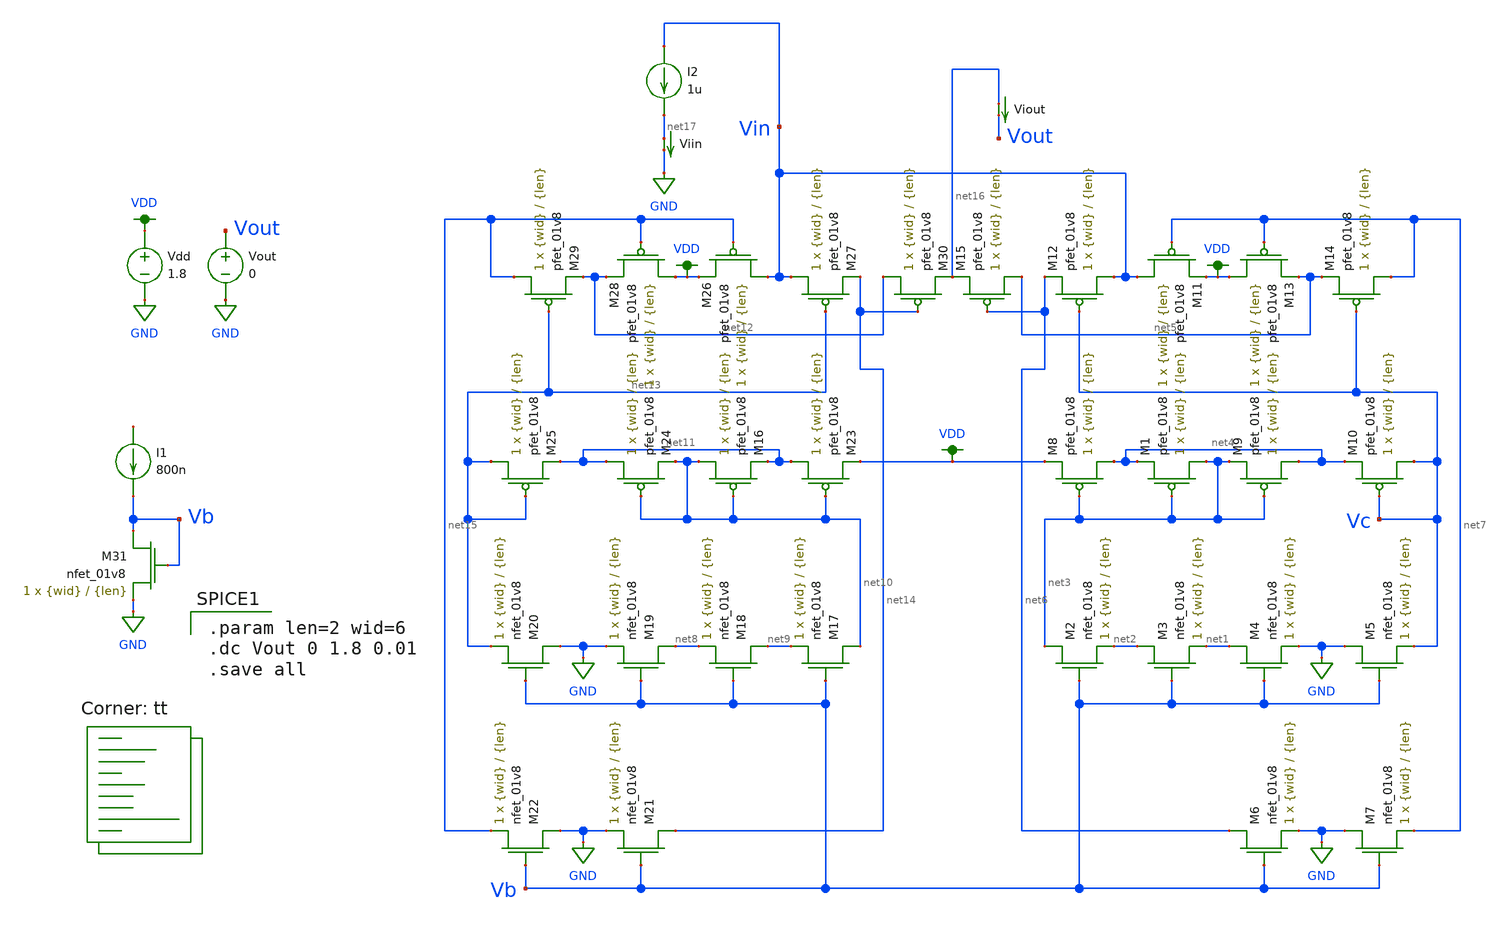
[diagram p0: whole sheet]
** sch_path: mp3/mirror_lvs_tb.sch
**.subckt mirror_lvs_tb
XM1 net3 net3 net4 VDD sky130_fd_pr__pfet_01v8 L={len} W={wid} nf=1 ad='int((nf+1)/2) * W/nf * 0.29'
+ as='int((nf+2)/2) * W/nf * 0.29' pd='2*int((nf+1)/2) * (W/nf + 0.29)' ps='2*int((nf+2)/2) * (W/nf + 0.29)'
+ nrd='0.29 / W' nrs='0.29 / W' sa=0 sb=0 sd=0 mult=1 m=1
XM2 net3 Vb net2 GND sky130_fd_pr__nfet_01v8 L={len} W={wid} nf=1 ad='int((nf+1)/2) * W/nf * 0.29' as='int((nf+2)/2) * W/nf * 0.29'
+ pd='2*int((nf+1)/2) * (W/nf + 0.29)' ps='2*int((nf+2)/2) * (W/nf + 0.29)' nrd='0.29 / W' nrs='0.29 / W'
+ sa=0 sb=0 sd=0 mult=1 m=1
XM3 net2 Vb net1 GND sky130_fd_pr__nfet_01v8 L={len} W={wid} nf=1 ad='int((nf+1)/2) * W/nf * 0.29' as='int((nf+2)/2) * W/nf * 0.29'
+ pd='2*int((nf+1)/2) * (W/nf + 0.29)' ps='2*int((nf+2)/2) * (W/nf + 0.29)' nrd='0.29 / W' nrs='0.29 / W'
+ sa=0 sb=0 sd=0 mult=1 m=1
XM4 net1 Vb GND GND sky130_fd_pr__nfet_01v8 L={len} W={wid} nf=1 ad='int((nf+1)/2) * W/nf * 0.29' as='int((nf+2)/2) * W/nf * 0.29'
+ pd='2*int((nf+1)/2) * (W/nf + 0.29)' ps='2*int((nf+2)/2) * (W/nf + 0.29)' nrd='0.29 / W' nrs='0.29 / W'
+ sa=0 sb=0 sd=0 mult=1 m=1
XM5 GND Vb Vc GND sky130_fd_pr__nfet_01v8 L={len} W={wid} nf=1 ad='int((nf+1)/2) * W/nf * 0.29' as='int((nf+2)/2) * W/nf * 0.29'
+ pd='2*int((nf+1)/2) * (W/nf + 0.29)' ps='2*int((nf+2)/2) * (W/nf + 0.29)' nrd='0.29 / W' nrs='0.29 / W'
+ sa=0 sb=0 sd=0 mult=1 m=1
XM6 net6 Vb GND GND sky130_fd_pr__nfet_01v8 L={len} W={wid} nf=1 ad='int((nf+1)/2) * W/nf * 0.29' as='int((nf+2)/2) * W/nf * 0.29'
+ pd='2*int((nf+1)/2) * (W/nf + 0.29)' ps='2*int((nf+2)/2) * (W/nf + 0.29)' nrd='0.29 / W' nrs='0.29 / W'
+ sa=0 sb=0 sd=0 mult=1 m=1
XM7 GND Vb net7 GND sky130_fd_pr__nfet_01v8 L={len} W={wid} nf=1 ad='int((nf+1)/2) * W/nf * 0.29' as='int((nf+2)/2) * W/nf * 0.29'
+ pd='2*int((nf+1)/2) * (W/nf + 0.29)' ps='2*int((nf+2)/2) * (W/nf + 0.29)' nrd='0.29 / W' nrs='0.29 / W'
+ sa=0 sb=0 sd=0 mult=1 m=1
XM8 net4 net3 VDD VDD sky130_fd_pr__pfet_01v8 L={len} W={wid} nf=1 ad='int((nf+1)/2) * W/nf * 0.29' as='int((nf+2)/2) * W/nf * 0.29'
+ pd='2*int((nf+1)/2) * (W/nf + 0.29)' ps='2*int((nf+2)/2) * (W/nf + 0.29)' nrd='0.29 / W' nrs='0.29 / W'
+ sa=0 sb=0 sd=0 mult=1 m=1
XM9 net4 net3 net3 VDD sky130_fd_pr__pfet_01v8 L={len} W={wid} nf=1 ad='int((nf+1)/2) * W/nf * 0.29'
+ as='int((nf+2)/2) * W/nf * 0.29' pd='2*int((nf+1)/2) * (W/nf + 0.29)' ps='2*int((nf+2)/2) * (W/nf + 0.29)'
+ nrd='0.29 / W' nrs='0.29 / W' sa=0 sb=0 sd=0 mult=1 m=1
XM10 Vc Vc net4 VDD sky130_fd_pr__pfet_01v8 L={len} W={wid} nf=1 ad='int((nf+1)/2) * W/nf * 0.29' as='int((nf+2)/2) * W/nf * 0.29'
+ pd='2*int((nf+1)/2) * (W/nf + 0.29)' ps='2*int((nf+2)/2) * (W/nf + 0.29)' nrd='0.29 / W' nrs='0.29 / W'
+ sa=0 sb=0 sd=0 mult=1 m=1
XM11 Vin net7 VDD VDD sky130_fd_pr__pfet_01v8 L={len} W={wid} nf=1 ad='int((nf+1)/2) * W/nf * 0.29' as='int((nf+2)/2) * W/nf * 0.29'
+ pd='2*int((nf+1)/2) * (W/nf + 0.29)' ps='2*int((nf+2)/2) * (W/nf + 0.29)' nrd='0.29 / W' nrs='0.29 / W'
+ sa=0 sb=0 sd=0 mult=1 m=1
XM12 Vin Vc net6 VDD sky130_fd_pr__pfet_01v8 L={len} W={wid} nf=1 ad='int((nf+1)/2) * W/nf * 0.29' as='int((nf+2)/2) * W/nf * 0.29'
+ pd='2*int((nf+1)/2) * (W/nf + 0.29)' ps='2*int((nf+2)/2) * (W/nf + 0.29)' nrd='0.29 / W' nrs='0.29 / W'
+ sa=0 sb=0 sd=0 mult=1 m=1
XM13 VDD net7 net5 VDD sky130_fd_pr__pfet_01v8 L={len} W={wid} nf=1 ad='int((nf+1)/2) * W/nf * 0.29'
+ as='int((nf+2)/2) * W/nf * 0.29' pd='2*int((nf+1)/2) * (W/nf + 0.29)' ps='2*int((nf+2)/2) * (W/nf + 0.29)'
+ nrd='0.29 / W' nrs='0.29 / W' sa=0 sb=0 sd=0 mult=1 m=1
XM14 net7 Vc net5 VDD sky130_fd_pr__pfet_01v8 L={len} W={wid} nf=1 ad='int((nf+1)/2) * W/nf * 0.29' as='int((nf+2)/2) * W/nf * 0.29'
+ pd='2*int((nf+1)/2) * (W/nf + 0.29)' ps='2*int((nf+2)/2) * (W/nf + 0.29)' nrd='0.29 / W' nrs='0.29 / W'
+ sa=0 sb=0 sd=0 mult=1 m=1
XM15 net5 net6 net16 VDD sky130_fd_pr__pfet_01v8 L={len} W={wid} nf=1 ad='int((nf+1)/2) * W/nf * 0.29'
+ as='int((nf+2)/2) * W/nf * 0.29' pd='2*int((nf+1)/2) * (W/nf + 0.29)' ps='2*int((nf+2)/2) * (W/nf + 0.29)'
+ nrd='0.29 / W' nrs='0.29 / W' sa=0 sb=0 sd=0 mult=1 m=1
XM16 net10 net10 net11 VDD sky130_fd_pr__pfet_01v8 L={len} W={wid} nf=1 ad='int((nf+1)/2) * W/nf * 0.29'
+ as='int((nf+2)/2) * W/nf * 0.29' pd='2*int((nf+1)/2) * (W/nf + 0.29)' ps='2*int((nf+2)/2) * (W/nf + 0.29)'
+ nrd='0.29 / W' nrs='0.29 / W' sa=0 sb=0 sd=0 mult=1 m=1
XM17 net10 Vb net9 GND sky130_fd_pr__nfet_01v8 L={len} W={wid} nf=1 ad='int((nf+1)/2) * W/nf * 0.29'
+ as='int((nf+2)/2) * W/nf * 0.29' pd='2*int((nf+1)/2) * (W/nf + 0.29)' ps='2*int((nf+2)/2) * (W/nf + 0.29)'
+ nrd='0.29 / W' nrs='0.29 / W' sa=0 sb=0 sd=0 mult=1 m=1
XM18 net9 Vb net8 GND sky130_fd_pr__nfet_01v8 L={len} W={wid} nf=1 ad='int((nf+1)/2) * W/nf * 0.29' as='int((nf+2)/2) * W/nf * 0.29'
+ pd='2*int((nf+1)/2) * (W/nf + 0.29)' ps='2*int((nf+2)/2) * (W/nf + 0.29)' nrd='0.29 / W' nrs='0.29 / W'
+ sa=0 sb=0 sd=0 mult=1 m=1
XM19 net8 Vb GND GND sky130_fd_pr__nfet_01v8 L={len} W={wid} nf=1 ad='int((nf+1)/2) * W/nf * 0.29' as='int((nf+2)/2) * W/nf * 0.29'
+ pd='2*int((nf+1)/2) * (W/nf + 0.29)' ps='2*int((nf+2)/2) * (W/nf + 0.29)' nrd='0.29 / W' nrs='0.29 / W'
+ sa=0 sb=0 sd=0 mult=1 m=1
XM20 GND Vb net13 GND sky130_fd_pr__nfet_01v8 L={len} W={wid} nf=1 ad='int((nf+1)/2) * W/nf * 0.29' as='int((nf+2)/2) * W/nf * 0.29'
+ pd='2*int((nf+1)/2) * (W/nf + 0.29)' ps='2*int((nf+2)/2) * (W/nf + 0.29)' nrd='0.29 / W' nrs='0.29 / W'
+ sa=0 sb=0 sd=0 mult=1 m=1
XM21 net14 Vb GND GND sky130_fd_pr__nfet_01v8 L={len} W={wid} nf=1 ad='int((nf+1)/2) * W/nf * 0.29' as='int((nf+2)/2) * W/nf * 0.29'
+ pd='2*int((nf+1)/2) * (W/nf + 0.29)' ps='2*int((nf+2)/2) * (W/nf + 0.29)' nrd='0.29 / W' nrs='0.29 / W'
+ sa=0 sb=0 sd=0 mult=1 m=1
XM22 GND Vb net15 GND sky130_fd_pr__nfet_01v8 L={len} W={wid} nf=1 ad='int((nf+1)/2) * W/nf * 0.29' as='int((nf+2)/2) * W/nf * 0.29'
+ pd='2*int((nf+1)/2) * (W/nf + 0.29)' ps='2*int((nf+2)/2) * (W/nf + 0.29)' nrd='0.29 / W' nrs='0.29 / W'
+ sa=0 sb=0 sd=0 mult=1 m=1
XM23 net11 net10 VDD VDD sky130_fd_pr__pfet_01v8 L={len} W={wid} nf=1 ad='int((nf+1)/2) * W/nf * 0.29'
+ as='int((nf+2)/2) * W/nf * 0.29' pd='2*int((nf+1)/2) * (W/nf + 0.29)' ps='2*int((nf+2)/2) * (W/nf + 0.29)'
+ nrd='0.29 / W' nrs='0.29 / W' sa=0 sb=0 sd=0 mult=1 m=1
XM24 net11 net10 net10 VDD sky130_fd_pr__pfet_01v8 L={len} W={wid} nf=1 ad='int((nf+1)/2) * W/nf * 0.29'
+ as='int((nf+2)/2) * W/nf * 0.29' pd='2*int((nf+1)/2) * (W/nf + 0.29)' ps='2*int((nf+2)/2) * (W/nf + 0.29)'
+ nrd='0.29 / W' nrs='0.29 / W' sa=0 sb=0 sd=0 mult=1 m=1
XM25 net13 net13 net11 VDD sky130_fd_pr__pfet_01v8 L={len} W={wid} nf=1 ad='int((nf+1)/2) * W/nf * 0.29'
+ as='int((nf+2)/2) * W/nf * 0.29' pd='2*int((nf+1)/2) * (W/nf + 0.29)' ps='2*int((nf+2)/2) * (W/nf + 0.29)'
+ nrd='0.29 / W' nrs='0.29 / W' sa=0 sb=0 sd=0 mult=1 m=1
XM26 Vin net15 VDD VDD sky130_fd_pr__pfet_01v8 L={len} W={wid} nf=1 ad='int((nf+1)/2) * W/nf * 0.29'
+ as='int((nf+2)/2) * W/nf * 0.29' pd='2*int((nf+1)/2) * (W/nf + 0.29)' ps='2*int((nf+2)/2) * (W/nf + 0.29)'
+ nrd='0.29 / W' nrs='0.29 / W' sa=0 sb=0 sd=0 mult=1 m=1
XM27 Vin net13 net14 VDD sky130_fd_pr__pfet_01v8 L={len} W={wid} nf=1 ad='int((nf+1)/2) * W/nf * 0.29'
+ as='int((nf+2)/2) * W/nf * 0.29' pd='2*int((nf+1)/2) * (W/nf + 0.29)' ps='2*int((nf+2)/2) * (W/nf + 0.29)'
+ nrd='0.29 / W' nrs='0.29 / W' sa=0 sb=0 sd=0 mult=1 m=1
XM28 VDD net15 net12 VDD sky130_fd_pr__pfet_01v8 L={len} W={wid} nf=1 ad='int((nf+1)/2) * W/nf * 0.29'
+ as='int((nf+2)/2) * W/nf * 0.29' pd='2*int((nf+1)/2) * (W/nf + 0.29)' ps='2*int((nf+2)/2) * (W/nf + 0.29)'
+ nrd='0.29 / W' nrs='0.29 / W' sa=0 sb=0 sd=0 mult=1 m=1
XM29 net15 net13 net12 VDD sky130_fd_pr__pfet_01v8 L={len} W={wid} nf=1 ad='int((nf+1)/2) * W/nf * 0.29'
+ as='int((nf+2)/2) * W/nf * 0.29' pd='2*int((nf+1)/2) * (W/nf + 0.29)' ps='2*int((nf+2)/2) * (W/nf + 0.29)'
+ nrd='0.29 / W' nrs='0.29 / W' sa=0 sb=0 sd=0 mult=1 m=1
XM30 net12 net14 net16 VDD sky130_fd_pr__pfet_01v8 L={len} W={wid} nf=1 ad='int((nf+1)/2) * W/nf * 0.29'
+ as='int((nf+2)/2) * W/nf * 0.29' pd='2*int((nf+1)/2) * (W/nf + 0.29)' ps='2*int((nf+2)/2) * (W/nf + 0.29)'
+ nrd='0.29 / W' nrs='0.29 / W' sa=0 sb=0 sd=0 mult=1 m=1
Vdd VDD GND 1.8
I1 net18 Vb 800n
XM31 Vb Vb GND GND sky130_fd_pr__nfet_01v8 L={len} W={wid} nf=1 ad='int((nf+1)/2) * W/nf * 0.29' as='int((nf+2)/2) * W/nf * 0.29'
+ pd='2*int((nf+1)/2) * (W/nf + 0.29)' ps='2*int((nf+2)/2) * (W/nf + 0.29)' nrd='0.29 / W' nrs='0.29 / W'
+ sa=0 sb=0 sd=0 mult=1 m=1
I2 Vin net17 1u
Vout Vout GND 0
Viout net16 Vout 0
.save i(viout)
Viin net17 GND 0
.save i(viin)
**** begin user architecture code
.lib $::SKYWATER_MODELS/sky130.lib.spice tt

.param len=2 wid=6
.dc Vout 0 1.8 0.01
.save all


**** end user architecture code
**.ends
.GLOBAL GND
.GLOBAL VDD
.end
